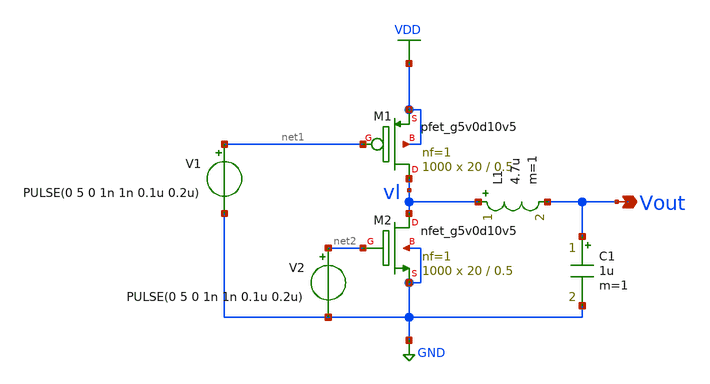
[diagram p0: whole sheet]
** sch_path: Ene_Thompson/Buck.sch
**.subckt Buck Vout
*.opin Vout
XM1 vl net1 VDD VDD sky130_fd_pr__pfet_g5v0d10v5 L=0.5 W=20 nf=1 ad='int((nf+1)/2) * W/nf * 0.29' as='int((nf+2)/2) * W/nf * 0.29'
+ pd='2*int((nf+1)/2) * (W/nf + 0.29)' ps='2*int((nf+2)/2) * (W/nf + 0.29)' nrd='0.29 / W' nrs='0.29 / W'
+ sa=0 sb=0 sd=0 mult=1000 m=1000
XM2 vl net2 GND GND sky130_fd_pr__nfet_g5v0d10v5 L=0.5 W=20 nf=1 ad='int((nf+1)/2) * W/nf * 0.29' as='int((nf+2)/2) * W/nf * 0.29'
+ pd='2*int((nf+1)/2) * (W/nf + 0.29)' ps='2*int((nf+2)/2) * (W/nf + 0.29)' nrd='0.29 / W' nrs='0.29 / W'
+ sa=0 sb=0 sd=0 mult=1000 m=1000
L1 vl Vout 4.7u m=1
C1 Vout GND 1u m=1
V1 net1 GND PULSE(0 5 0 1n 1n 0.1u 0.2u)
V2 net2 GND PULSE(0 5 0 1n 1n 0.1u 0.2u)
**.ends
.GLOBAL GND
.GLOBAL VDD
.end
